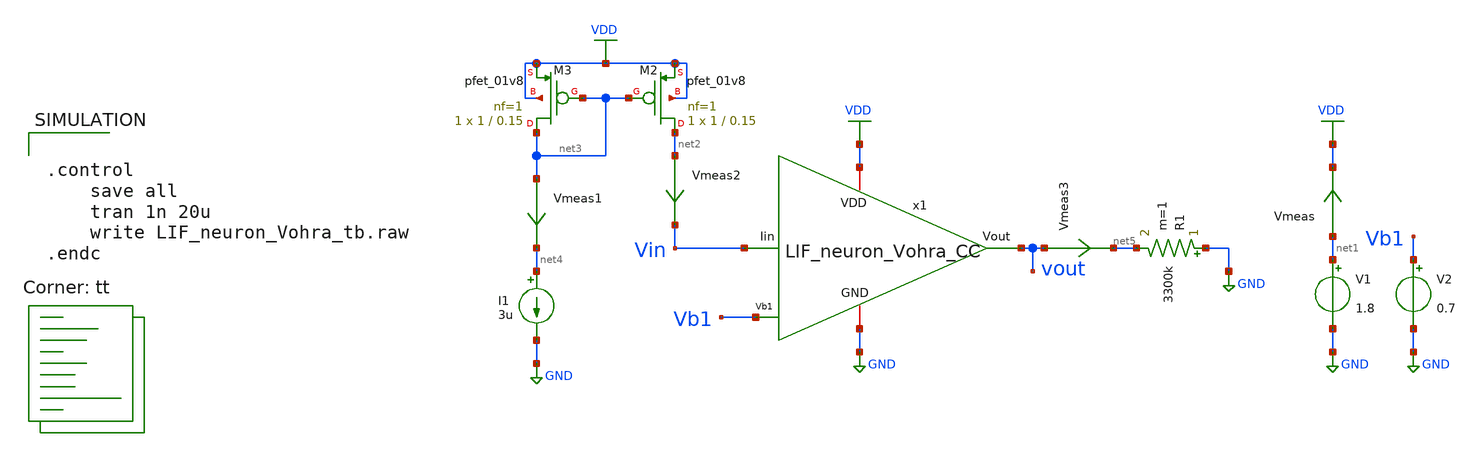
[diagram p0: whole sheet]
** sch_path: LIF_neuron/LIF_neuron_Vohra_CC_tb.sch
**.subckt LIF_neuron_Vohra_CC_tb
V1 net1 GND 1.8
V2 Vb1 GND 0.7
x1 VDD vout Vb1 GND Vin LIF_neuron_Vohra_CC
I1 net4 GND 3u
XM2 net2 net3 VDD VDD sky130_fd_pr__pfet_01v8 L=0.15 W=1 nf=1 ad='int((nf+1)/2) * W/nf * 0.29' as='int((nf+2)/2) * W/nf * 0.29'
+ pd='2*int((nf+1)/2) * (W/nf + 0.29)' ps='2*int((nf+2)/2) * (W/nf + 0.29)' nrd='0.29 / W' nrs='0.29 / W'
+ sa=0 sb=0 sd=0 mult=1 m=1
XM3 net3 net3 VDD VDD sky130_fd_pr__pfet_01v8 L=0.15 W=1 nf=1 ad='int((nf+1)/2) * W/nf * 0.29' as='int((nf+2)/2) * W/nf * 0.29'
+ pd='2*int((nf+1)/2) * (W/nf + 0.29)' ps='2*int((nf+2)/2) * (W/nf + 0.29)' nrd='0.29 / W' nrs='0.29 / W'
+ sa=0 sb=0 sd=0 mult=1 m=1
Vmeas net1 VDD 0
.save i(vmeas)
Vmeas1 net3 net4 0
.save i(vmeas1)
Vmeas2 net2 Vin 0
.save i(vmeas2)
Vmeas3 vout net5 0
.save i(vmeas3)
R1 GND net5 3300k m=1
**** begin user architecture code


.control
	save all
	tran 1n 20u
	write LIF_neuron_Vohra_tb.raw
.endc


.lib $::SKYWATER_MODELS/sky130.lib.spice tt
**** end user architecture code
**.ends

* expanding   symbol:  /home/ricardo/RATT_repos/Proyectos_xschem/LIF_neuron/LIF_neuron_Vohra_CC.sym
*+ # of pins=5
** sym_path: LIF_neuron/LIF_neuron_Vohra_CC.sym
** sch_path: LIF_neuron/LIF_neuron_Vohra_CC.sch
.subckt LIF_neuron_Vohra_CC VDD Vout Vb1 GND Iin
*.iopin GND
*.ipin Vb1
*.iopin VDD
*.opin Vout
*.ipin Iin
XM8 Ve Vb1 GND GND sky130_fd_pr__nfet_01v8 L=0.5 W=5 nf=1 ad='int((nf+1)/2) * W/nf * 0.29' as='int((nf+2)/2) * W/nf * 0.29'
+ pd='2*int((nf+1)/2) * (W/nf + 0.29)' ps='2*int((nf+2)/2) * (W/nf + 0.29)' nrd='0.29 / W' nrs='0.29 / W'
+ sa=0 sb=0 sd=0 mult=1 m=1
XM7 Vd Va Ve GND sky130_fd_pr__nfet_01v8 L=1 W=1 nf=1 ad='int((nf+1)/2) * W/nf * 0.29' as='int((nf+2)/2) * W/nf * 0.29'
+ pd='2*int((nf+1)/2) * (W/nf + 0.29)' ps='2*int((nf+2)/2) * (W/nf + 0.29)' nrd='0.29 / W' nrs='0.29 / W'
+ sa=0 sb=0 sd=0 mult=1 m=1
XM6 Vd Va VDD VDD sky130_fd_pr__pfet_01v8 L=1 W=1 nf=1 ad='int((nf+1)/2) * W/nf * 0.29' as='int((nf+2)/2) * W/nf * 0.29'
+ pd='2*int((nf+1)/2) * (W/nf + 0.29)' ps='2*int((nf+2)/2) * (W/nf + 0.29)' nrd='0.29 / W' nrs='0.29 / W'
+ sa=0 sb=0 sd=0 mult=1 m=1
XCr Vd GND sky130_fd_pr__cap_mim_m3_1 W=10 L=1 MF=1 m=1
XM9 Iin Vd GND GND sky130_fd_pr__nfet_01v8 L=10 W=1 nf=1 ad='int((nf+1)/2) * W/nf * 0.29' as='int((nf+2)/2) * W/nf * 0.29'
+ pd='2*int((nf+1)/2) * (W/nf + 0.29)' ps='2*int((nf+2)/2) * (W/nf + 0.29)' nrd='0.29 / W' nrs='0.29 / W'
+ sa=0 sb=0 sd=0 mult=1 m=1
XCm Iin GND sky130_fd_pr__cap_mim_m3_1 W=151 L=1 MF=50 m=50
XM5 Vc Vout GND GND sky130_fd_pr__nfet_01v8 L=0.5 W=1 nf=1 ad='int((nf+1)/2) * W/nf * 0.29' as='int((nf+2)/2) * W/nf * 0.29'
+ pd='2*int((nf+1)/2) * (W/nf + 0.29)' ps='2*int((nf+2)/2) * (W/nf + 0.29)' nrd='0.29 / W' nrs='0.29 / W'
+ sa=0 sb=0 sd=0 mult=1 m=1
XM3 Va Iin Vc GND sky130_fd_pr__nfet_01v8 L=1 W=1 nf=1 ad='int((nf+1)/2) * W/nf * 0.29' as='int((nf+2)/2) * W/nf * 0.29'
+ pd='2*int((nf+1)/2) * (W/nf + 0.29)' ps='2*int((nf+2)/2) * (W/nf + 0.29)' nrd='0.29 / W' nrs='0.29 / W'
+ sa=0 sb=0 sd=0 mult=1 m=1
XM1 Va Iin VDD VDD sky130_fd_pr__pfet_01v8 L=1 W=1 nf=1 ad='int((nf+1)/2) * W/nf * 0.29' as='int((nf+2)/2) * W/nf * 0.29'
+ pd='2*int((nf+1)/2) * (W/nf + 0.29)' ps='2*int((nf+2)/2) * (W/nf + 0.29)' nrd='0.29 / W' nrs='0.29 / W'
+ sa=0 sb=0 sd=0 mult=1 m=1
XM4 Vout Va Vc GND sky130_fd_pr__nfet_01v8 L=1 W=1 nf=1 ad='int((nf+1)/2) * W/nf * 0.29' as='int((nf+2)/2) * W/nf * 0.29'
+ pd='2*int((nf+1)/2) * (W/nf + 0.29)' ps='2*int((nf+2)/2) * (W/nf + 0.29)' nrd='0.29 / W' nrs='0.29 / W'
+ sa=0 sb=0 sd=0 mult=1 m=1
XM2 Vout Va VDD VDD sky130_fd_pr__pfet_01v8 L=1 W=1 nf=1 ad='int((nf+1)/2) * W/nf * 0.29' as='int((nf+2)/2) * W/nf * 0.29'
+ pd='2*int((nf+1)/2) * (W/nf + 0.29)' ps='2*int((nf+2)/2) * (W/nf + 0.29)' nrd='0.29 / W' nrs='0.29 / W'
+ sa=0 sb=0 sd=0 mult=1 m=1
.ends

.GLOBAL GND
.GLOBAL VDD
.end
